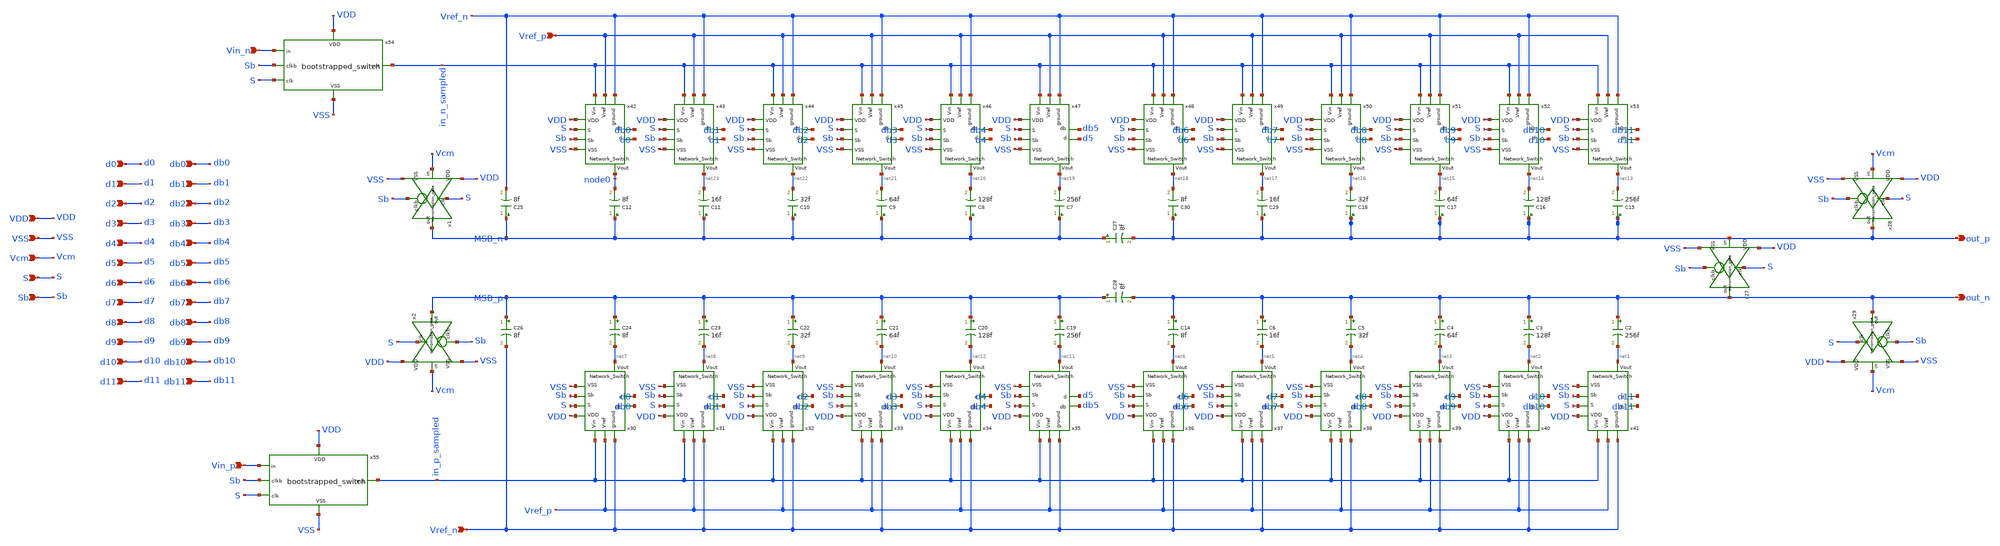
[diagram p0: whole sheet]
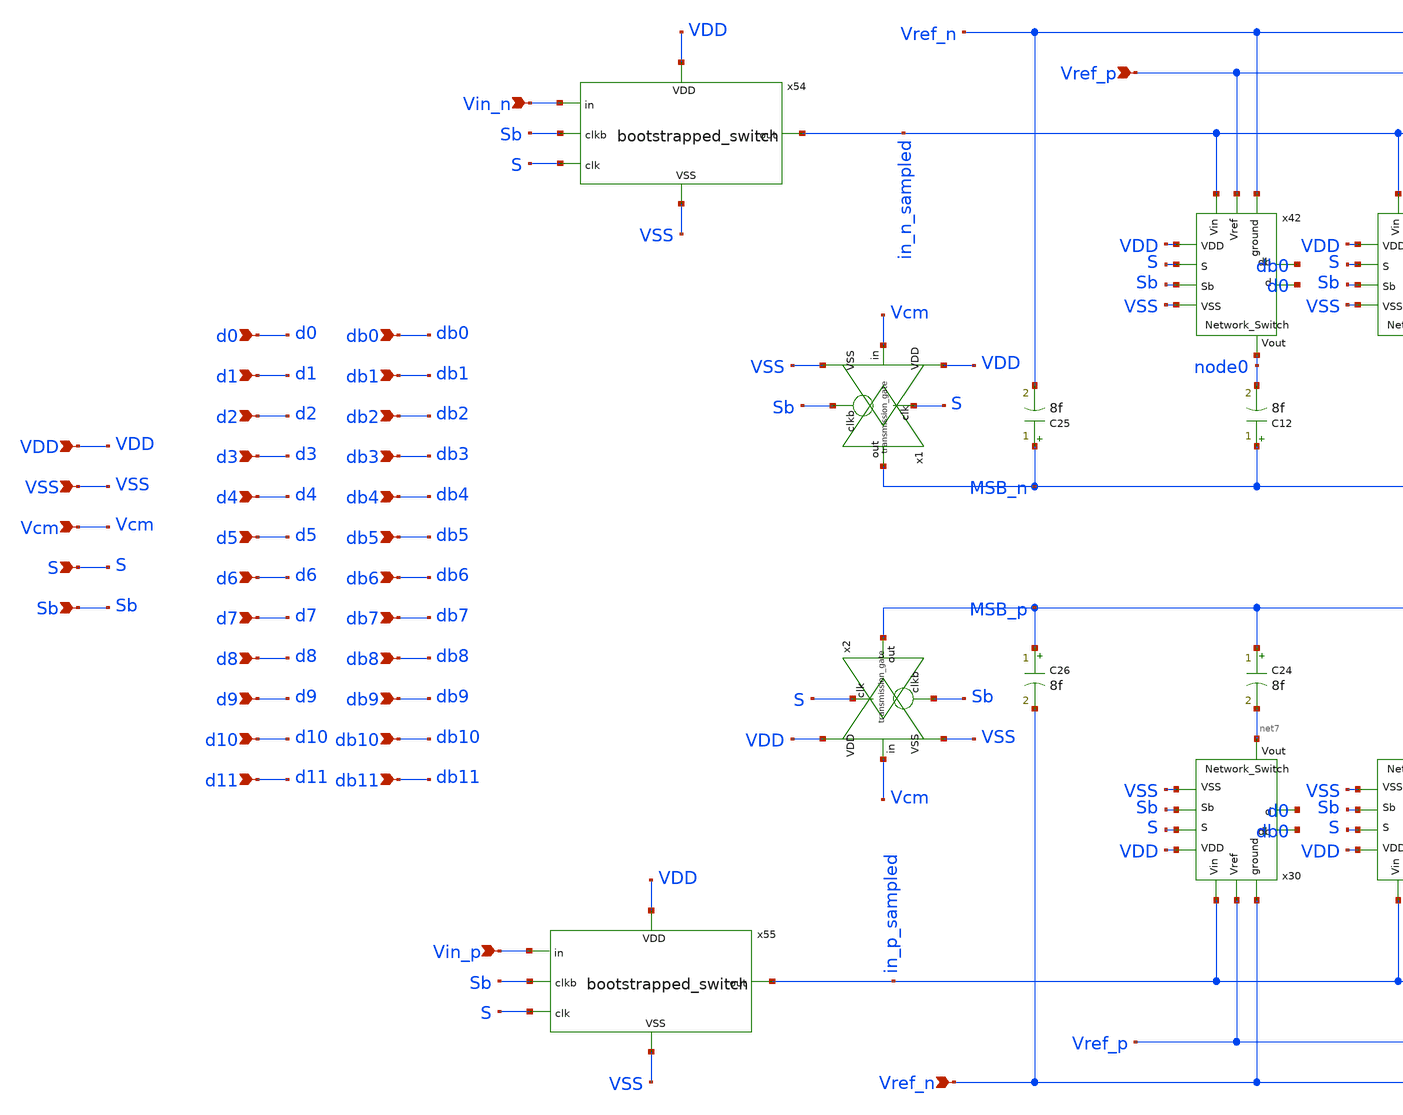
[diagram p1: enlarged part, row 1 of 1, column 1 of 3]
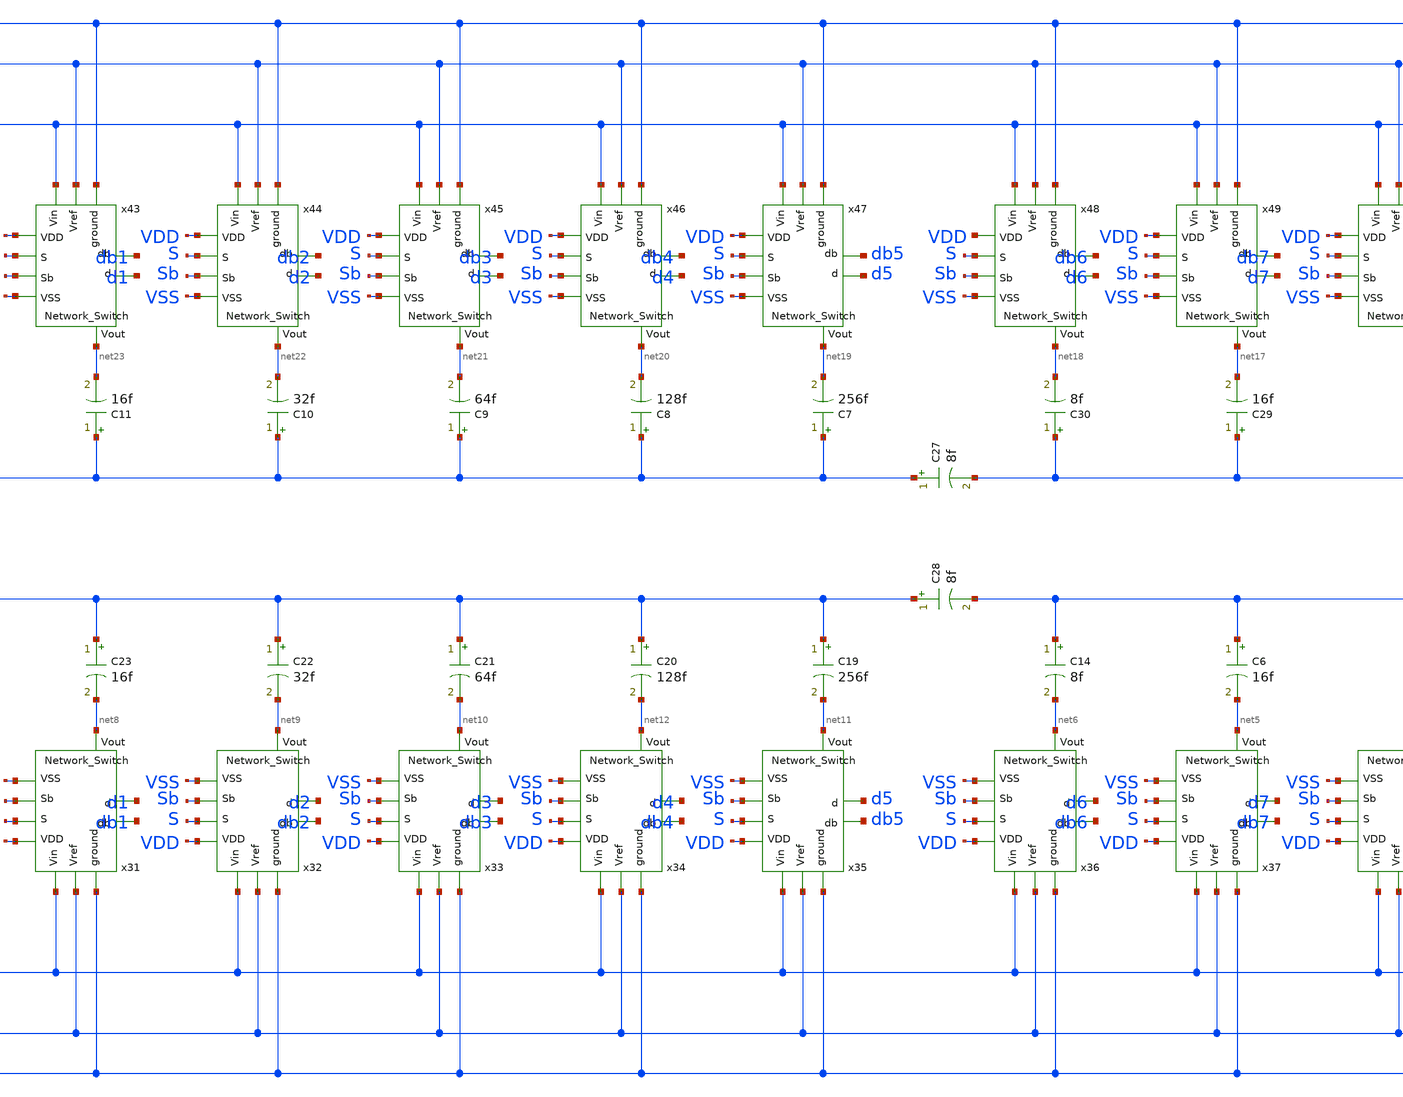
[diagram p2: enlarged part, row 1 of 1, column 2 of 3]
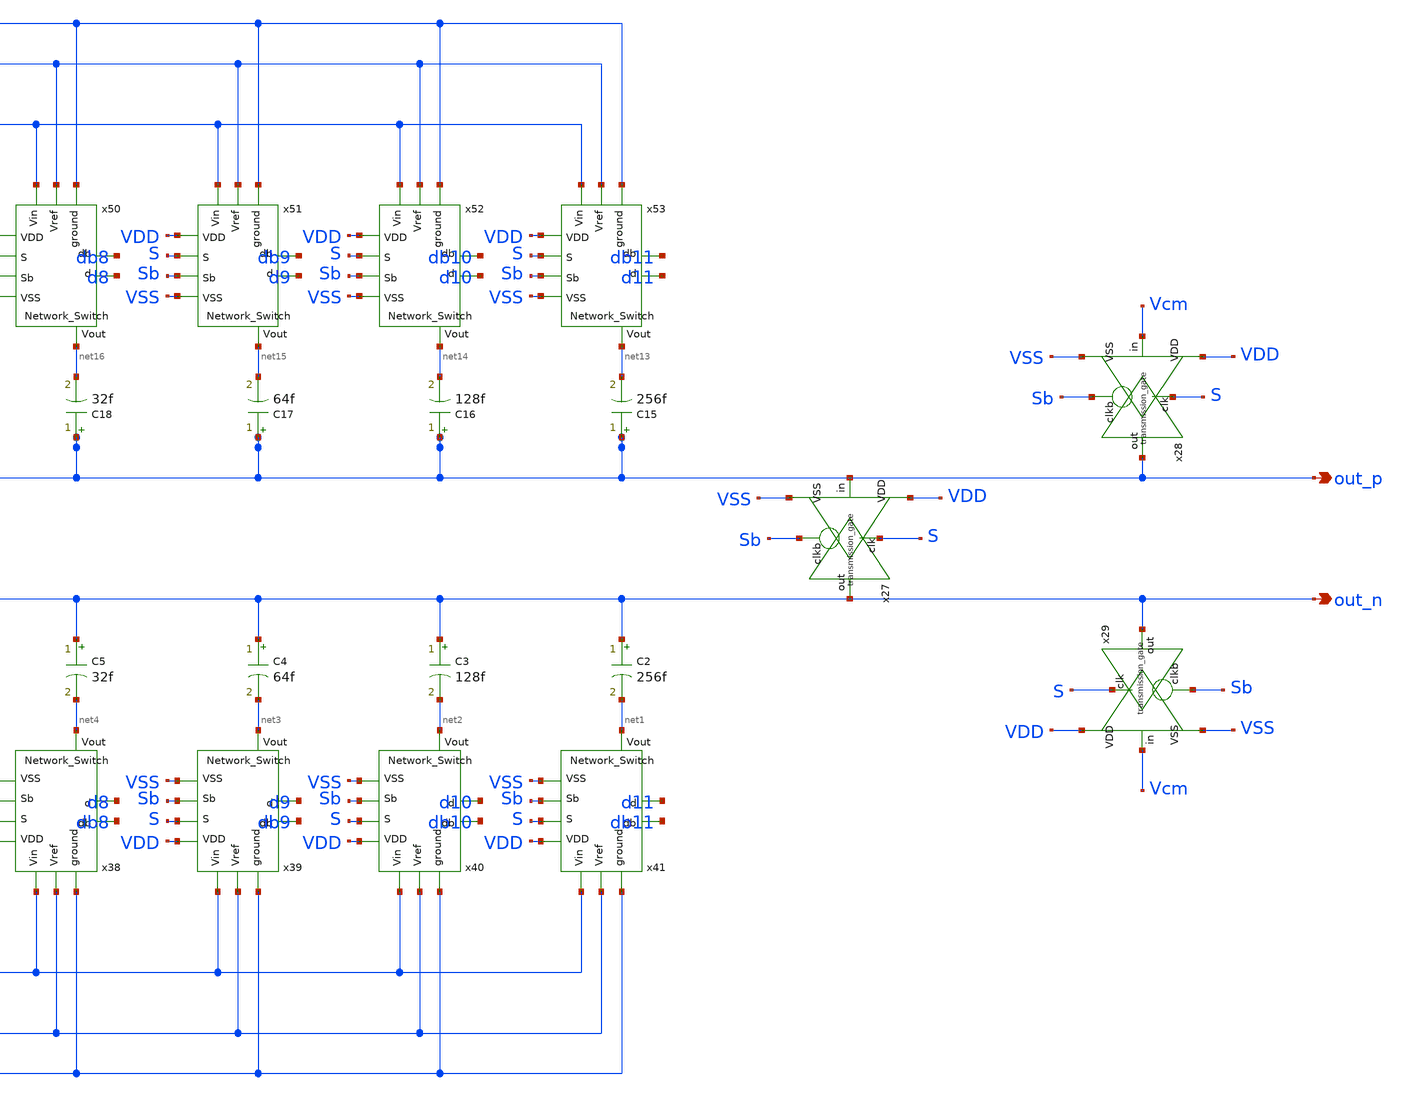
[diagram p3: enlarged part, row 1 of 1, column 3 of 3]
** sch_path: CAP_DAC_ideal.sch
**.subckt CAP_DAC_ideal VDD VSS S Sb d3 db3 Vcm out_p out_n Vref_p Vref_n d0 db0 d1 db1 d2 db2 d5
*+ db5 d4 db4 d7 db7 d6 db6 d9 db9 d8 db8 d11 db11 d10 db10 Vin_n Vin_p
*.ipin VDD
*.ipin VSS
*.ipin S
*.ipin Sb
*.ipin d3
*.ipin db3
*.ipin Vcm
*.opin out_p
*.opin out_n
*.ipin Vref_p
*.ipin Vref_n
*.ipin d0
*.ipin db0
*.ipin d1
*.ipin db1
*.ipin d2
*.ipin db2
*.ipin d5
*.ipin db5
*.ipin d4
*.ipin db4
*.ipin d7
*.ipin db7
*.ipin d6
*.ipin db6
*.ipin d9
*.ipin db9
*.ipin d8
*.ipin db8
*.ipin d11
*.ipin db11
*.ipin d10
*.ipin db10
*.ipin Vin_n
*.ipin Vin_p
x28 Vcm Sb S VDD VSS out_p transmission_gate
x29 Vcm Sb S VDD VSS out_n transmission_gate
x30 VDD Vref_n Vref_p VSS S Sb d0 db0 in_p_sampled net7 Network_Switch
x31 VDD Vref_n Vref_p VSS S Sb d1 db1 in_p_sampled net8 Network_Switch
x32 VDD Vref_n Vref_p VSS S Sb d2 db2 in_p_sampled net9 Network_Switch
x33 VDD Vref_n Vref_p VSS S Sb d3 db3 in_p_sampled net10 Network_Switch
x34 VDD Vref_n Vref_p VSS S Sb d4 db4 in_p_sampled net12 Network_Switch
x35 VDD Vref_n Vref_p VSS S Sb d5 db5 in_p_sampled net11 Network_Switch
x36 VDD Vref_n Vref_p VSS S Sb d6 db6 in_p_sampled net6 Network_Switch
x37 VDD Vref_n Vref_p VSS S Sb d7 db7 in_p_sampled net5 Network_Switch
x38 VDD Vref_n Vref_p VSS S Sb d8 db8 in_p_sampled net4 Network_Switch
x39 VDD Vref_n Vref_p VSS S Sb d9 db9 in_p_sampled net3 Network_Switch
x40 VDD Vref_n Vref_p VSS S Sb d10 db10 in_p_sampled net2 Network_Switch
x41 VDD Vref_n Vref_p VSS S Sb d11 db11 in_p_sampled net1 Network_Switch
x42 VDD Vref_n Vref_p VSS S Sb d0 db0 in_n_sampled node0 Network_Switch
x43 VDD Vref_n Vref_p VSS S Sb d1 db1 in_n_sampled net23 Network_Switch
x44 VDD Vref_n Vref_p VSS S Sb d2 db2 in_n_sampled net22 Network_Switch
x45 VDD Vref_n Vref_p VSS S Sb d3 db3 in_n_sampled net21 Network_Switch
x46 VDD Vref_n Vref_p VSS S Sb d4 db4 in_n_sampled net20 Network_Switch
x47 VDD Vref_n Vref_p VSS S Sb d5 db5 in_n_sampled net19 Network_Switch
x48 VDD Vref_n Vref_p VSS S Sb d6 db6 in_n_sampled net18 Network_Switch
x49 VDD Vref_n Vref_p VSS S Sb d7 db7 in_n_sampled net17 Network_Switch
x50 VDD Vref_n Vref_p VSS S Sb d8 db8 in_n_sampled net16 Network_Switch
x51 VDD Vref_n Vref_p VSS S Sb d9 db9 in_n_sampled net15 Network_Switch
x52 VDD Vref_n Vref_p VSS S Sb d10 db10 in_n_sampled net14 Network_Switch
x53 VDD Vref_n Vref_p VSS S Sb d11 db11 in_n_sampled net13 Network_Switch
x54 VDD Vin_n Sb S in_n_sampled VSS bootstrapped_switch
x55 VDD Vin_p Sb S in_p_sampled VSS bootstrapped_switch
x27 out_p Sb S VDD VSS out_n transmission_gate
C7 MSB_n net19 256f m=1
C8 MSB_n net20 128f m=1
C9 MSB_n net21 64f m=1
C10 MSB_n net22 32f m=1
C11 MSB_n net23 16f m=1
C12 MSB_n node0 8f m=1
C19 MSB_p net11 256f m=1
C20 MSB_p net12 128f m=1
C21 MSB_p net10 64f m=1
C22 MSB_p net9 32f m=1
C23 MSB_p net8 16f m=1
C24 MSB_p net7 8f m=1
C25 MSB_n Vref_n 8f m=1
C26 MSB_p Vref_n 8f m=1
C27 MSB_n out_p 8f m=1
C28 MSB_p out_n 8f m=1
C2 out_n net1 256f m=1
C3 out_n net2 128f m=1
C4 out_n net3 64f m=1
C5 out_n net4 32f m=1
C6 out_n net5 16f m=1
C14 out_n net6 8f m=1
C15 out_p net13 256f m=1
C16 out_p net14 128f m=1
C17 out_p net15 64f m=1
C18 out_p net16 32f m=1
C29 out_p net17 16f m=1
C30 out_p net18 8f m=1
x1 Vcm Sb S VDD VSS MSB_n transmission_gate
x2 Vcm Sb S VDD VSS MSB_p transmission_gate
**.ends

* expanding   symbol:  project/transmission_gate.sym # of pins=6
** sym_path: transmission_gate.sym
** sch_path: transmission_gate.sch
.subckt transmission_gate in clkb clk VDD VSS out
*.ipin in
*.ipin clk
*.ipin clkb
*.opin out
*.ipin VDD
*.ipin VSS
XM1 out clk in VSS sky130_fd_pr__nfet_01v8 L=0.15 W=0.5 nf=1 ad='int((nf+1)/2) * W/nf * 0.29' as='int((nf+2)/2) * W/nf * 0.29'
+ pd='2*int((nf+1)/2) * (W/nf + 0.29)' ps='2*int((nf+2)/2) * (W/nf + 0.29)' nrd='0.29 / W' nrs='0.29 / W'
+ sa=0 sb=0 sd=0 mult=1 m=1
XM2 out clkb in VDD sky130_fd_pr__pfet_01v8 L=0.15 W=0.5 nf=1 ad='int((nf+1)/2) * W/nf * 0.29' as='int((nf+2)/2) * W/nf * 0.29'
+ pd='2*int((nf+1)/2) * (W/nf + 0.29)' ps='2*int((nf+2)/2) * (W/nf + 0.29)' nrd='0.29 / W' nrs='0.29 / W'
+ sa=0 sb=0 sd=0 mult=1 m=1
.ends


* expanding   symbol:  project/Network_Switch.sym # of pins=10
** sym_path: Network_Switch.sym
** sch_path: Network_Switch.sch
.subckt Network_Switch VDD ground Vref VSS S Sb d db Vin Vout
*.ipin ground
*.ipin Vref
*.ipin Vin
*.opin Vout
*.ipin VDD
*.ipin VSS
*.ipin S
*.ipin Sb
*.ipin d
*.ipin db
x1 ground d db VDD VSS net1 transmission_gate
x2 Vref db d VDD VSS net1 transmission_gate
x3 net1 S Sb VDD VSS Vout transmission_gate
x4 Vin Sb S VDD VSS Vout transmission_gate
.ends


* expanding   symbol:  project/bootstrapped_switch.sym # of pins=6
** sym_path: bootstrapped_switch.sym
** sch_path: bootstrapped_switch.sch
.subckt bootstrapped_switch VDD in clkb clk out VSS
*.ipin in
*.opin out
*.ipin VSS
*.ipin VDD
*.ipin clkb
*.ipin clk
XM1 net4 clkb net5 net5 sky130_fd_pr__nfet_01v8 L=0.15 W=2 nf=1 ad='int((nf+1)/2) * W/nf * 0.29' as='int((nf+2)/2) * W/nf * 0.29'
+ pd='2*int((nf+1)/2) * (W/nf + 0.29)' ps='2*int((nf+2)/2) * (W/nf + 0.29)' nrd='0.29 / W' nrs='0.29 / W'
+ sa=0 sb=0 sd=0 mult=1 m=1
XM2 in Vg net4 VSS sky130_fd_pr__nfet_01v8 L=1 W=0.5 nf=1 ad='int((nf+1)/2) * W/nf * 0.29' as='int((nf+2)/2) * W/nf * 0.29'
+ pd='2*int((nf+1)/2) * (W/nf + 0.29)' ps='2*int((nf+2)/2) * (W/nf + 0.29)' nrd='0.29 / W' nrs='0.29 / W'
+ sa=0 sb=0 sd=0 mult=1 m=1
XM3 Vp Vg net1 Vp sky130_fd_pr__pfet_01v8 L=0.15 W=2 nf=1 ad='int((nf+1)/2) * W/nf * 0.29' as='int((nf+2)/2) * W/nf * 0.29'
+ pd='2*int((nf+1)/2) * (W/nf + 0.29)' ps='2*int((nf+2)/2) * (W/nf + 0.29)' nrd='0.29 / W' nrs='0.29 / W'
+ sa=0 sb=0 sd=0 mult=1 m=1
XM5 out Vg in VSS sky130_fd_pr__nfet_01v8 L=0.15 W=30 nf=1 ad='int((nf+1)/2) * W/nf * 0.29' as='int((nf+2)/2) * W/nf * 0.29'
+ pd='2*int((nf+1)/2) * (W/nf + 0.29)' ps='2*int((nf+2)/2) * (W/nf + 0.29)' nrd='0.29 / W' nrs='0.29 / W'
+ sa=0 sb=0 sd=0 mult=1 m=1
XM6 out clkb in VDD sky130_fd_pr__pfet_01v8 L=0.15 W=30 nf=1 ad='int((nf+1)/2) * W/nf * 0.29' as='int((nf+2)/2) * W/nf * 0.29'
+ pd='2*int((nf+1)/2) * (W/nf + 0.29)' ps='2*int((nf+2)/2) * (W/nf + 0.29)' nrd='0.29 / W' nrs='0.29 / W'
+ sa=0 sb=0 sd=0 mult=1 m=1
XM8 net6 clkb net2 net2 sky130_fd_pr__nfet_01v8 L=0.15 W=0.5 nf=1 ad='int((nf+1)/2) * W/nf * 0.29' as='int((nf+2)/2) * W/nf * 0.29'
+ pd='2*int((nf+1)/2) * (W/nf + 0.29)' ps='2*int((nf+2)/2) * (W/nf + 0.29)' nrd='0.29 / W' nrs='0.29 / W'
+ sa=0 sb=0 sd=0 mult=1 m=1
XC1 net4 Vp sky130_fd_pr__cap_mim_m3_1 W=18 L=18 MF=10 m=10
XM7 Vg VDD net6 net6 sky130_fd_pr__nfet_01v8 L=0.15 W=0.5 nf=1 ad='int((nf+1)/2) * W/nf * 0.29' as='int((nf+2)/2) * W/nf * 0.29'
+ pd='2*int((nf+1)/2) * (W/nf + 0.29)' ps='2*int((nf+2)/2) * (W/nf + 0.29)' nrd='0.29 / W' nrs='0.29 / W'
+ sa=0 sb=0 sd=0 mult=1 m=1
XM4 Vg net3 Vp Vp sky130_fd_pr__pfet_01v8 L=0.15 W=0.5 nf=1 ad='int((nf+1)/2) * W/nf * 0.29' as='int((nf+2)/2) * W/nf * 0.29'
+ pd='2*int((nf+1)/2) * (W/nf + 0.29)' ps='2*int((nf+2)/2) * (W/nf + 0.29)' nrd='0.29 / W' nrs='0.29 / W'
+ sa=0 sb=0 sd=0 mult=1 m=1
XC2 out VSS sky130_fd_pr__cap_mim_m3_1 W=36 L=36 MF=20 m=20
XM10 net1 clk net7 net1 sky130_fd_pr__pfet_01v8 L=0.15 W=2 nf=1 ad='int((nf+1)/2) * W/nf * 0.29' as='int((nf+2)/2) * W/nf * 0.29'
+ pd='2*int((nf+1)/2) * (W/nf + 0.29)' ps='2*int((nf+2)/2) * (W/nf + 0.29)' nrd='0.29 / W' nrs='0.29 / W'
+ sa=0 sb=0 sd=0 mult=1 m=1
XM11 net5 clkb net8 net8 sky130_fd_pr__nfet_01v8 L=0.15 W=2 nf=1 ad='int((nf+1)/2) * W/nf * 0.29' as='int((nf+2)/2) * W/nf * 0.29'
+ pd='2*int((nf+1)/2) * (W/nf + 0.29)' ps='2*int((nf+2)/2) * (W/nf + 0.29)' nrd='0.29 / W' nrs='0.29 / W'
+ sa=0 sb=0 sd=0 mult=1 m=1
XM12 net7 clk VDD net7 sky130_fd_pr__pfet_01v8 L=0.15 W=2 nf=1 ad='int((nf+1)/2) * W/nf * 0.29' as='int((nf+2)/2) * W/nf * 0.29'
+ pd='2*int((nf+1)/2) * (W/nf + 0.29)' ps='2*int((nf+2)/2) * (W/nf + 0.29)' nrd='0.29 / W' nrs='0.29 / W'
+ sa=0 sb=0 sd=0 mult=1 m=1
XM13 net8 clkb VSS VSS sky130_fd_pr__nfet_01v8 L=0.15 W=2 nf=1 ad='int((nf+1)/2) * W/nf * 0.29' as='int((nf+2)/2) * W/nf * 0.29'
+ pd='2*int((nf+1)/2) * (W/nf + 0.29)' ps='2*int((nf+2)/2) * (W/nf + 0.29)' nrd='0.29 / W' nrs='0.29 / W'
+ sa=0 sb=0 sd=0 mult=1 m=1
XM14 net2 clkb VSS VSS sky130_fd_pr__nfet_01v8 L=0.15 W=0.5 nf=1 ad='int((nf+1)/2) * W/nf * 0.29' as='int((nf+2)/2) * W/nf * 0.29'
+ pd='2*int((nf+1)/2) * (W/nf + 0.29)' ps='2*int((nf+2)/2) * (W/nf + 0.29)' nrd='0.29 / W' nrs='0.29 / W'
+ sa=0 sb=0 sd=0 mult=1 m=1
XM15 net3 clk VDD VDD sky130_fd_pr__pfet_01v8 L=0.15 W=1 nf=1 ad='int((nf+1)/2) * W/nf * 0.29' as='int((nf+2)/2) * W/nf * 0.29'
+ pd='2*int((nf+1)/2) * (W/nf + 0.29)' ps='2*int((nf+2)/2) * (W/nf + 0.29)' nrd='0.29 / W' nrs='0.29 / W'
+ sa=0 sb=0 sd=0 mult=1 m=1
XM16 net3 clk net4 VSS sky130_fd_pr__nfet_01v8 L=1 W=0.5 nf=1 ad='int((nf+1)/2) * W/nf * 0.29' as='int((nf+2)/2) * W/nf * 0.29'
+ pd='2*int((nf+1)/2) * (W/nf + 0.29)' ps='2*int((nf+2)/2) * (W/nf + 0.29)' nrd='0.29 / W' nrs='0.29 / W'
+ sa=0 sb=0 sd=0 mult=1 m=1
XM17 net3 Vg net4 VSS sky130_fd_pr__nfet_01v8 L=0.15 W=2 nf=1 ad='int((nf+1)/2) * W/nf * 0.29' as='int((nf+2)/2) * W/nf * 0.29'
+ pd='2*int((nf+1)/2) * (W/nf + 0.29)' ps='2*int((nf+2)/2) * (W/nf + 0.29)' nrd='0.29 / W' nrs='0.29 / W'
+ sa=0 sb=0 sd=0 mult=1 m=1
.ends

.end
